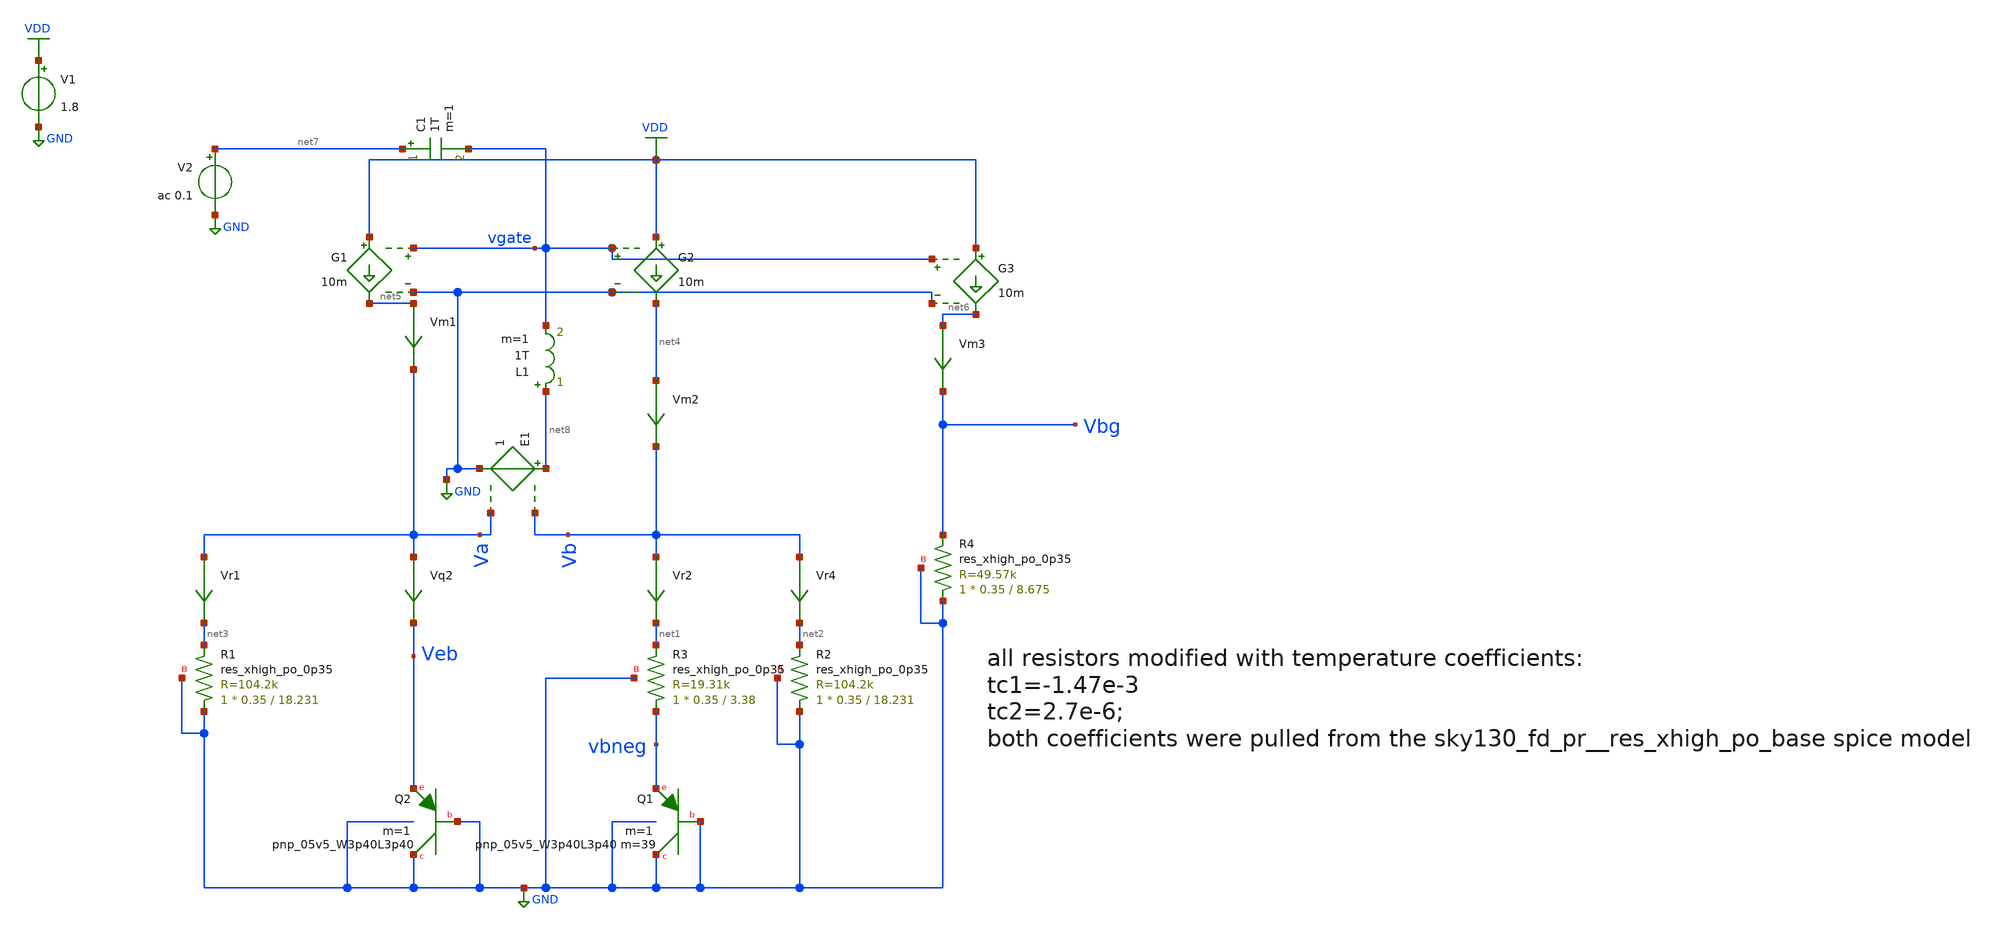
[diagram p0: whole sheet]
** sch_path: schematics/tsmc_bandgap_ideal_feedback_pdk_res.sch
**.subckt tsmc_bandgap_ideal_feedback_pdk_res
XQ2 GND GND Veb sky130_fd_pr__pnp_05v5_W3p40L3p40 m=1
V1 VDD GND 1.8
Vr4 Vb net2 0
.save i(vr4)
Vr2 Vb net1 0
.save i(vr2)
Vm1 net5 Va 0
.save i(vm1)
Vm2 net4 Vb 0
.save i(vm2)
Vm3 net6 Vbg 0
.save i(vm3)
Vr1 Va net3 0
.save i(vr1)
Vq2 Va Veb 0
.save i(vq2)
XQ1 GND GND vbneg sky130_fd_pr__pnp_05v5_W3p40L3p40 m=39 m=1
E1 net8 GND Vb Va 1
G1 VDD net5 vgate GND 10m
L1 net8 vgate 1T m=1
C1 net7 vgate 1T m=1
V2 net7 GND ac 0.1
G2 VDD net4 vgate GND 10m
G3 VDD net6 vgate GND 10m
XR1 GND net3 GND sky130_fd_pr__res_xhigh_po_0p35 L=18.231 mult=1 m=1
XR2 GND net2 GND sky130_fd_pr__res_xhigh_po_0p35 L=18.231 mult=1 m=1
XR3 vbneg net1 GND sky130_fd_pr__res_xhigh_po_0p35 L=3.38 mult=1 m=1
XR4 GND Vbg GND sky130_fd_pr__res_xhigh_po_0p35 L=8.675 mult=1 m=1
**** begin user architecture code

.include $::SKYWATER_MODELS/cells/nfet_01v8/sky130_fd_pr__nfet_01v8__tt.corner.spice
.include $::SKYWATER_MODELS/cells/nfet_01v8_lvt/sky130_fd_pr__nfet_01v8_lvt__tt.corner.spice
.include $::SKYWATER_MODELS/cells/pfet_01v8/sky130_fd_pr__pfet_01v8__tt.corner.spice
.include $::SKYWATER_MODELS/cells/nfet_03v3_nvt/sky130_fd_pr__nfet_03v3_nvt__tt.corner.spice
.include $::SKYWATER_MODELS/cells/nfet_05v0_nvt/sky130_fd_pr__nfet_05v0_nvt__tt.corner.spice
.include $::SKYWATER_MODELS/cells/esd_nfet_01v8/sky130_fd_pr__esd_nfet_01v8__tt.corner.spice
.include $::SKYWATER_MODELS/cells/pfet_01v8_lvt/sky130_fd_pr__pfet_01v8_lvt__tt.corner.spice
.include $::SKYWATER_MODELS/cells/pfet_01v8_hvt/sky130_fd_pr__pfet_01v8_hvt__tt.corner.spice
.include $::SKYWATER_MODELS/cells/esd_pfet_g5v0d10v5/sky130_fd_pr__esd_pfet_g5v0d10v5__tt.corner.spice
.include $::SKYWATER_MODELS/cells/pfet_g5v0d10v5/sky130_fd_pr__pfet_g5v0d10v5__tt.corner.spice
.include $::SKYWATER_MODELS/cells/pfet_g5v0d16v0/sky130_fd_pr__pfet_g5v0d16v0__tt.corner.spice
.include $::SKYWATER_MODELS/cells/nfet_g5v0d10v5/sky130_fd_pr__nfet_g5v0d10v5__tt.corner.spice
.include $::SKYWATER_MODELS/cells/nfet_g5v0d16v0/sky130_fd_pr__nfet_g5v0d16v0__tt_discrete.corner.spice
.include $::SKYWATER_MODELS/cells/esd_nfet_g5v0d10v5/sky130_fd_pr__esd_nfet_g5v0d10v5__tt.corner.spice
.include $::SKYWATER_MODELS/models/corners/tt/nonfet.spice
* Mismatch parameters
.include $::SKYWATER_MODELS/cells/nfet_01v8/sky130_fd_pr__nfet_01v8__mismatch.corner.spice
.include $::SKYWATER_MODELS/cells/pfet_01v8/sky130_fd_pr__pfet_01v8__mismatch.corner.spice
.include $::SKYWATER_MODELS/cells/nfet_01v8_lvt/sky130_fd_pr__nfet_01v8_lvt__mismatch.corner.spice
.include $::SKYWATER_MODELS/cells/pfet_01v8_lvt/sky130_fd_pr__pfet_01v8_lvt__mismatch.corner.spice
.include $::SKYWATER_MODELS/cells/pfet_01v8_hvt/sky130_fd_pr__pfet_01v8_hvt__mismatch.corner.spice
.include $::SKYWATER_MODELS/cells/nfet_g5v0d10v5/sky130_fd_pr__nfet_g5v0d10v5__mismatch.corner.spice
.include $::SKYWATER_MODELS/cells/pfet_g5v0d10v5/sky130_fd_pr__pfet_g5v0d10v5__mismatch.corner.spice
.include $::SKYWATER_MODELS/cells/nfet_05v0_nvt/sky130_fd_pr__nfet_05v0_nvt__mismatch.corner.spice
.include $::SKYWATER_MODELS/cells/nfet_03v3_nvt/sky130_fd_pr__nfet_03v3_nvt__mismatch.corner.spice
* Resistor$::SKYWATER_MODELS/Capacitor
.include $::SKYWATER_MODELS/models/r+c/res_typical__cap_typical.spice
.include $::SKYWATER_MODELS/models/r+c/res_typical__cap_typical__lin.spice
* Special cells
.include $::SKYWATER_MODELS/models/corners/tt/specialized_cells.spice
* All models
.include $::SKYWATER_MODELS/models/all.spice
.include $::SKYWATER_MODELS/cells/pnp_05v5/sky130_fd_pr__pnp_05v5_W3p40L3p40.model.spice
* Corner
.include $::SKYWATER_MODELS/models/corners/tt/rf.spice



.option savecurrents
.option warn=1
.param R3val=20k
.param alpha=1.12439
.param R2R3ratio='4.663181043*alpha'
.param R2val='R3val*R2R3ratio'
.param R4R2ratio=0.47924034354
.param R4val='R2val*R4R2ratio'
.control
save all
dc TEMP  -140 140 0.1
plot Vbg
plot deriv(Vbg)
let i = vm3#branch
let indx = 1670
*indx is the index of temperature sweep for 27degC
echo 'Vbg @ 27degC'
let vbg27c = vbg[indx]
print vbg27c
echo 'dVbe/degC & ppm @ 27degC'
print deriv(vbg)[indx] deriv(vbg)[indx]/vbg27c
plot deriv(vbg)/vbg27c
plot v(va, vb) vs i
plot vm1#branch vm2#branch vm3#branch
let vsg = vdd - vgate
let vsd1 = vdd - va
let vsd2 = vdd - vb
let vsd3 = vdd - vbg
let vth = @m.xm1.msky130_fd_pr__pfet_01v8['vth']
let vov = vsg - vth
plot vov vsd1 vsd2 vsd3
let deltav = vb - vbneg
let r4 =vbg/vm3#branch
let r1 =va/vr1#branch
let r2 =vb/vr4#branch
let r3 =deltav/vr2#branch
let vptat =(r2/r3*deltav)
plot veb vptat
plot deriv(veb) deriv(vptat)
let TCratio=deriv(veb)/deriv(vptat)
plot TCratio
plot vb - va
echo 'alpha correction factor'
let alpha=TCratio[indx]
print alpha
*let t=-140
*let tstop=140
*foreach t -140 -40 0 27 140
*option temp = $t
*ac dec 100 1 1e9
*let gainva=log10(abs(va/0.1))
*let gainvb=log10(abs(vb/0.1))
*let phaseb=(ph(vb/0.1)*180/pi)
*let phasea=(ph(va/0.1)*180/pi)
*plot gainva gainvb
*plot phasea phaseb
*end
.endc


**** end user architecture code
**.ends
.GLOBAL GND
.GLOBAL VDD
.end
